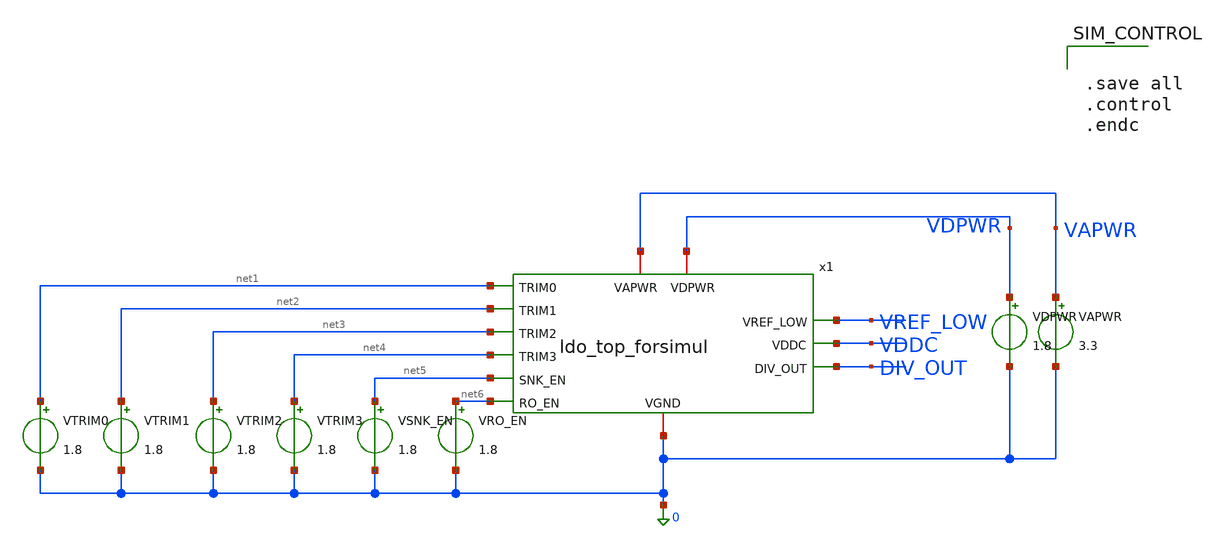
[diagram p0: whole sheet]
** sch_path: designs/bgr_ldo/ldo/ldo_top_tb.sch
**.subckt ldo_top_tb
VAPWR VAPWR 0 3.3
VDPWR VDPWR 0 1.8
VRO_EN net6 0 1.8
VSNK_EN net5 0 1.8
VTRIM3 net4 0 1.8
VTRIM2 net3 0 1.8
VTRIM1 net2 0 1.8
VTRIM0 net1 0 1.8
x1 VAPWR net1 VREF_LOW net2 net3 VDDC net4 net5 0 VDPWR DIV_OUT net6 ldo_top_forsimul
**** begin user architecture code

** opencircuitdesign pdks install
.lib $::SKYWATER_MODELS/sky130.lib.spice tt



.save all
.control
.endc

**** end user architecture code
**.ends
.end
